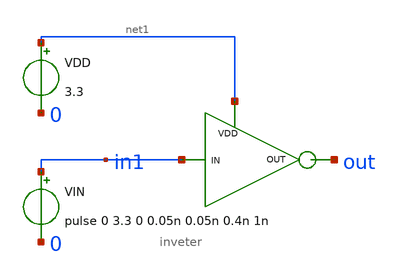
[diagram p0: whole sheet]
** sch_path: initial_notebooks_2023/Current-Steering DAC/DAC/Test_INV.sch
**.subckt Test_INV
x1 net1 out in1 inveter
VIN in1 0 pulse 0 3.3 0 0.05n 0.05n 0.4n 1n
VDD net1 0 3.3
**** begin user architecture code




.include /foss/pdks/gf180mcuC/libs.tech/ngspice/design.ngspice
.lib /foss/pdks/gf180mcuC/libs.tech/ngspice/sm141064.ngspice typical


.control
	*dc vin 0 3.3 0.01
	tran 1n 2n
	plot V(in1) V(out)
.endc
.save all




**** end user architecture code
**.ends
.end
